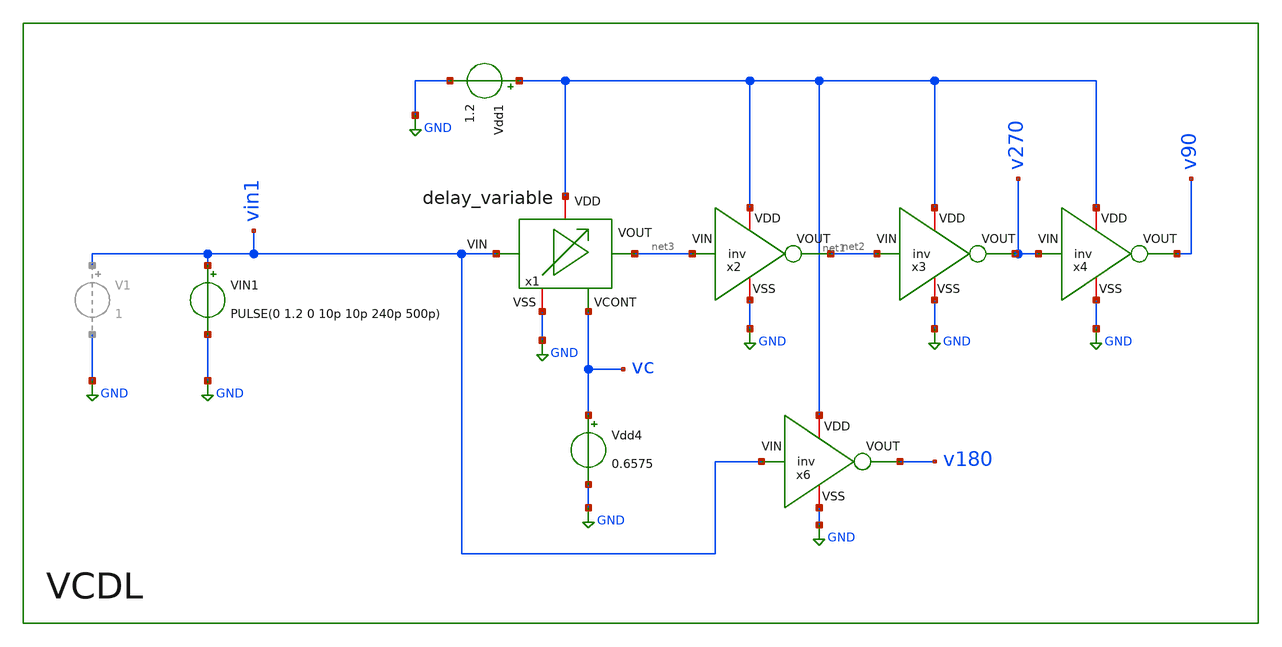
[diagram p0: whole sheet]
** sch_path: Clock_Gen/tb_QVDL_2GHZ.sch
**.subckt tb_QVDL_2GHZ
Vdd1 net1 GND 1.2
VIN1 vin1 GND PULSE(0 1.2 0 10p 10p 240p 500p)
Vdd4 vc GND 0.6575
x1 net1 vin1 net3 vc GND delay_variable
x2 net1 net2 net3 GND inv
x3 net1 v270 net2 GND inv
x4 net1 v90 v270 GND inv
x6 net1 v180 vin1 GND inv
**** begin user architecture code


.save v(vin1) v(v0) v(v90) v(v270) v(v180)

.tran 10p 3n
.save all

.control
run
set color0=white
write tran_logic.raw

* --- 1. MEDICIONES DE FASE Y RETARDO (Usando v90) ---
* Periodo Entrada (Ref)
meas tran T_per TRIG v(vin1) VAL=0.6 RISE=3 TARG v(vin1) VAL=0.6 RISE=4

* Retardo (Entrada vs v90)
meas tran T_del TRIG v(vin1) VAL=0.6 RISE=3 TARG v(v90) VAL=0.6 RISE=3

* Calculo Fase
let Phase_Deg = (T_del / T_per) * 360

print T_per
print T_del
print Phase_Deg


* --- 2. DUTY CYCLE (Usando v90) ---
* Periodo Salida
meas tran T_period TRIG v(v90) VAL=0.6 RISE=2 TARG v(v90) VAL=0.6 RISE=3

* Tiempo en ALTO (Ton)
* Desde que sube (RISE=2) hasta que baja (FALL=2)
meas tran T_high TRIG v(v90) VAL=0.6 RISE=2 TARG v(v90) VAL=0.6 FALL=2

* Tiempo en BAJO (Toff)
* Desde que baja (FALL=2) hasta que sube de nuevo (RISE=3)
meas tran T_low TRIG v(v90) VAL=0.6 FALL=2 TARG v(v90) VAL=0.6 RISE=3

let Duty_High = (T_high / T_period) * 100
let Duty_Low  = (T_low / T_period) * 100

print Duty_High
print Duty_Low
.endc



.lib cornerMOSlv.lib mos_tt
.include /foss/pdks/ihp-sg13g2/libs.ref/sg13g2_stdcell/spice/sg13g2_stdcell.spice


**** end user architecture code
**.ends

* expanding   symbol:  /foss/designs/PhaseInterpolator/2to4/delay_variable.sym # of pins=5
** sym_path: /foss/designs/PhaseInterpolator/2to4/delay_variable.sym
** sch_path: /foss/designs/PhaseInterpolator/2to4/delay_variable.sch
.subckt delay_variable VDD VIN VOUT VCONT VSS
*.iopin VSS
*.iopin VDD
*.opin VOUT
*.ipin VCONT
*.ipin VIN
XM1 VOUT VIN net2 VSS sg13_lv_nmos w=0.15u l=0.13u ng=1 m=4 mm_ok=1
XM2 net2 VCONT VSS VSS sg13_lv_nmos w=0.15u l=0.25u ng=1 m=4 mm_ok=1
XM3 net3 VCONT VSS VSS sg13_lv_nmos w=0.15u l=0.25u ng=1 m=5 mm_ok=1
XM5 VOUT VIN net1 VDD sg13_lv_pmos w=0.2u l=0.13u ng=1 m=5 mm_ok=1
XM6 net1 net3 VDD VDD sg13_lv_pmos w=0.2u l=0.25u ng=1 m=5 mm_ok=1
XM4 net3 net3 VDD VDD sg13_lv_pmos w=0.15u l=0.25u ng=1 m=5 mm_ok=1
.ends

.GLOBAL GND
.end
